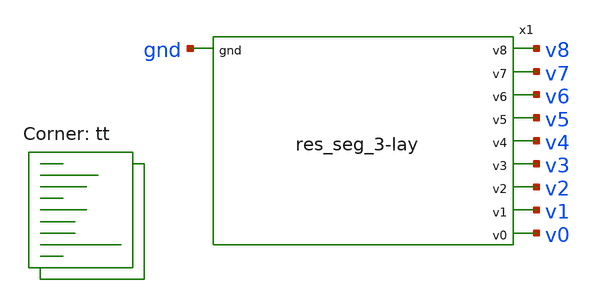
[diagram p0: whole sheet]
** sch_path: xschem/res_seg_3-lay-tb.sch
**.subckt res_seg_3-lay-tb
x1 v8 v7 v6 v5 v4 v3 v2 v1 v0 gnd res_seg_3-lay
**** begin user architecture code



  .include ~/10-bit-DAC/pex/res_seg_3.pex.spice
  .param max_freq=500e3 period={1/max_freq} time_high={period/2}
  .param delay_vin1={time_high} delay_vin2={time_high*1.5}
  .param lval=100u

  .option wnflag=1
  .option safecurrents

  V8 v8 gnd dc 4.2113
  v0 v0 gnd dc 3.8451
  *Vin  in  gnd pulse(0 1.8 {delay_vin1} 1p 1p {time_high} {period})
  *Vinb inb gnd pulse(1.8 0 {delay_vin1} 1p 1p {time_high} {period})

  .control
     reset
     save all
     tran 0.1n 100n
     write res_seg_3-lay-tb.raw
     set appendwrite

     *reset
     *save all
     *dc vref 0 1.8 0.1
     *write lvsf-tb.raw
*    quit 0
  .endc



.lib $::SKYWATER_MODELS/sky130.lib.spice tt
**** end user architecture code
**.ends
.end
